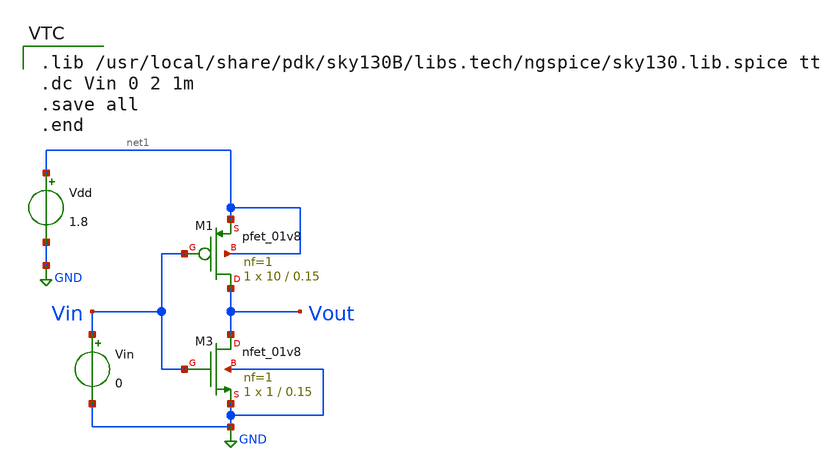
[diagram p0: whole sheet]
** sch_path: cmos_inverter_anaysis/voltage_transfer_characteristics/cmos_inverter.sch
**.subckt cmos_inverter
Vdd net1 GND 1.8
XM3 Vout Vin GND GND sky130_fd_pr__nfet_01v8 L=0.15 W=1 nf=1 ad='int((nf+1)/2) * W/nf * 0.29' as='int((nf+2)/2) * W/nf * 0.29'
+ pd='2*int((nf+1)/2) * (W/nf + 0.29)' ps='2*int((nf+2)/2) * (W/nf + 0.29)' nrd='0.29 / W' nrs='0.29 / W'
+ sa=0 sb=0 sd=0 mult=1 m=1
XM1 Vout Vin net1 net1 sky130_fd_pr__pfet_01v8 L=0.15 W=10 nf=1 ad='int((nf+1)/2) * W/nf * 0.29' as='int((nf+2)/2) * W/nf * 0.29'
+ pd='2*int((nf+1)/2) * (W/nf + 0.29)' ps='2*int((nf+2)/2) * (W/nf + 0.29)' nrd='0.29 / W' nrs='0.29 / W'
+ sa=0 sb=0 sd=0 mult=1 m=1
Vin Vin GND 0
**** begin user architecture code

.lib /usr/local/share/pdk/sky130B/libs.tech/ngspice/sky130.lib.spice tt
.dc Vin 0 2 1m
.save all
.end

**** end user architecture code
**.ends
.GLOBAL GND
.end
